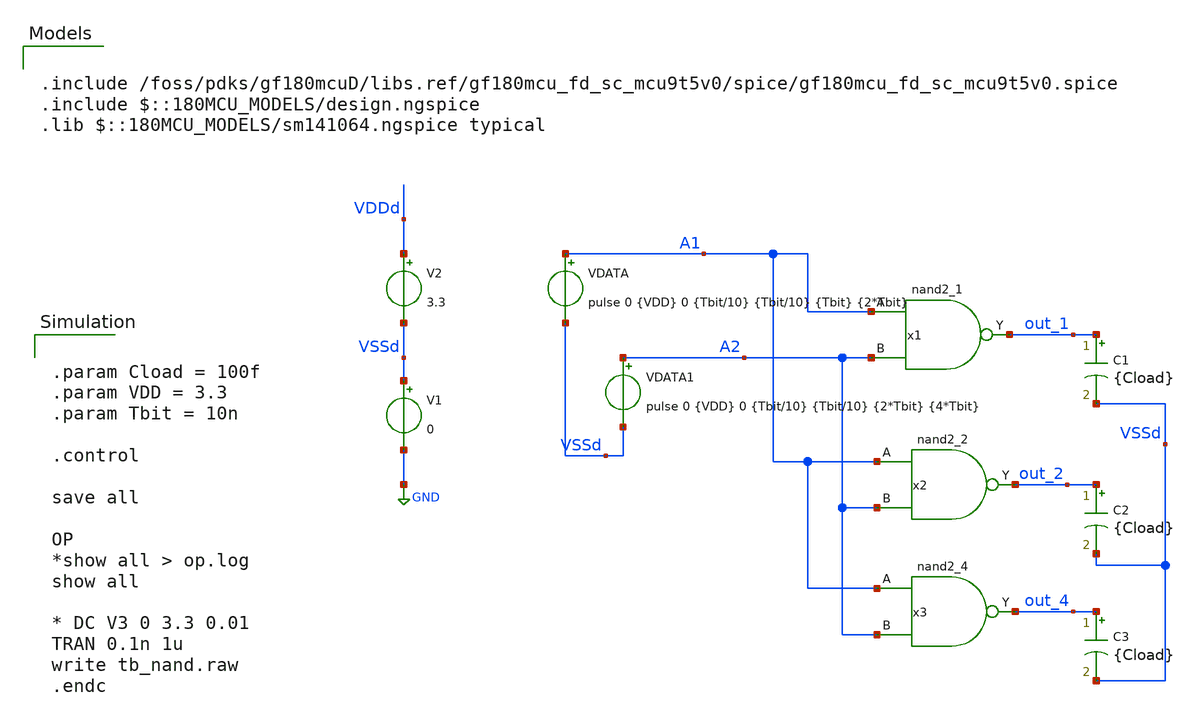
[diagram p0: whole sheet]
** sch_path: tb_digital_cells/tb_nand.sch
**.subckt tb_nand
V1 VSSd GND 0
V2 VDDd VSSd 3.3
x1 A1 A2 out_1 VDDd VDDd VSSd VSSd gf180mcu_fd_sc_mcu9t5v0__nand2_1
VDATA A1 VSSd pulse 0 {VDD} 0 {Tbit/10} {Tbit/10} {Tbit} {2*Tbit}
VDATA1 A2 VSSd pulse 0 {VDD} 0 {Tbit/10} {Tbit/10} {2*Tbit} {4*Tbit}
x2 A1 A2 out_2 VDDd VDDd VSSd VSSd gf180mcu_fd_sc_mcu9t5v0__nand2_2
x3 A1 A2 out_4 VDDd VDDd VSSd VSSd gf180mcu_fd_sc_mcu9t5v0__nand2_4
C1 out_1 VSSd {Cload} m=1
C2 out_2 VSSd {Cload} m=1
C3 out_4 VSSd {Cload} m=1
**** begin user architecture code


.param Cload = 100f
.param VDD = 3.3
.param Tbit = 10n

.control

save all

OP
*show all > op.log
show all

* DC V3 0 3.3 0.01
TRAN 0.1n 1u
write tb_nand.raw
.endc



.include /foss/pdks/gf180mcuD/libs.ref/gf180mcu_fd_sc_mcu9t5v0/spice/gf180mcu_fd_sc_mcu9t5v0.spice
.include $::180MCU_MODELS/design.ngspice
.lib $::180MCU_MODELS/sm141064.ngspice typical

**** end user architecture code
**.ends
.GLOBAL GND
.end
